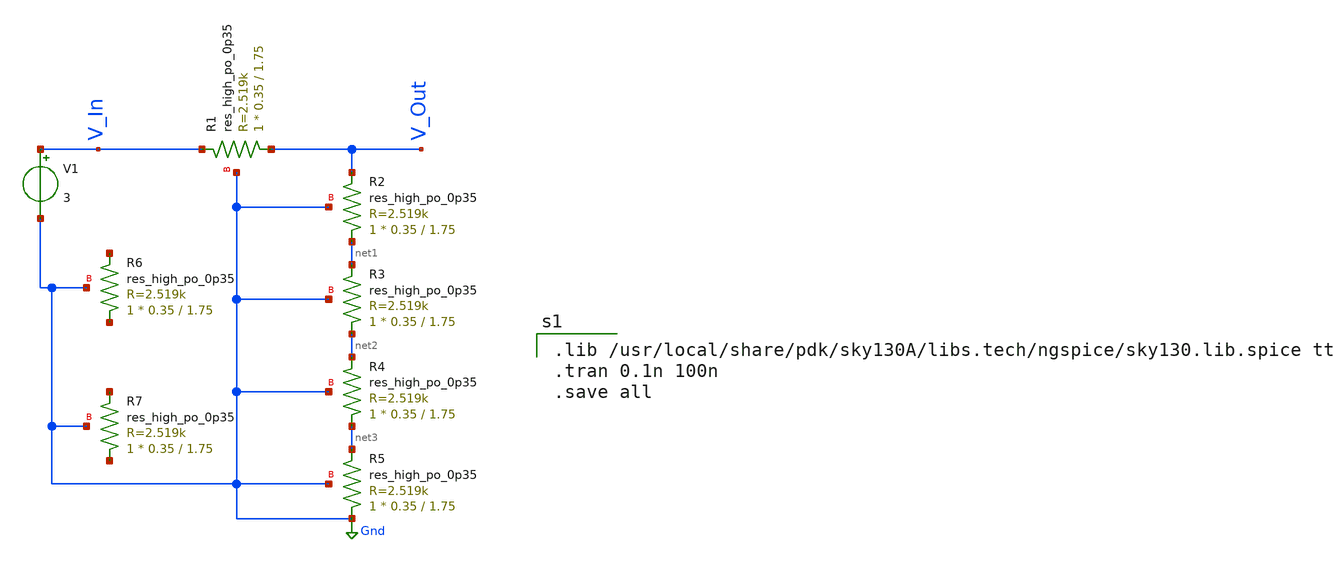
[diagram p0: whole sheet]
** sch_path: Schematic/VoltageDivider.sch
**.subckt VoltageDivider
XR2 net1 V_Out Gnd sky130_fd_pr__res_high_po_0p35 L=1.75 mult=1 m=1
XR3 net2 net1 Gnd sky130_fd_pr__res_high_po_0p35 L=1.75 mult=1 m=1
XR4 net3 net2 Gnd sky130_fd_pr__res_high_po_0p35 L=1.75 mult=1 m=1
XR5 Gnd net3 Gnd sky130_fd_pr__res_high_po_0p35 L=1.75 mult=1 m=1
XR6 net4 net5 Gnd sky130_fd_pr__res_high_po_0p35 L=1.75 mult=1 m=1
XR7 net6 net7 Gnd sky130_fd_pr__res_high_po_0p35 L=1.75 mult=1 m=1
XR1 V_Out V_In Gnd sky130_fd_pr__res_high_po_0p35 L=1.75 mult=1 m=1
V1 V_In Gnd 3
**** begin user architecture code

.lib /usr/local/share/pdk/sky130A/libs.tech/ngspice/sky130.lib.spice tt
.tran 0.1n 100n
.save all




**** end user architecture code
**.ends
.GLOBAL Gnd
.end
